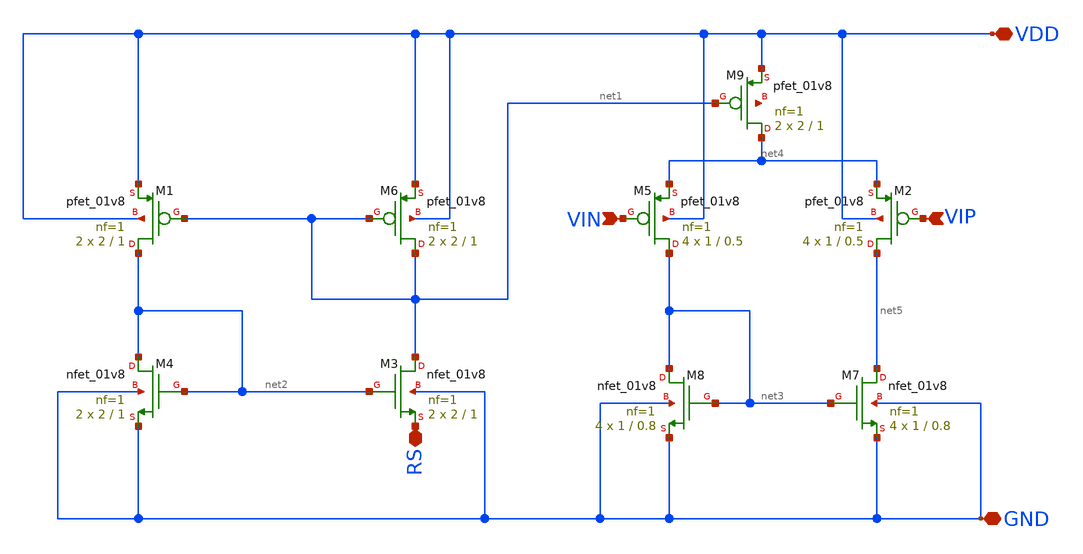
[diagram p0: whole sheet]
** sch_path: opamp/xschem/opamp.sch
**.subckt opamp GND VIP VIN RS VDD
*.iopin GND
*.ipin VIP
*.ipin VIN
*.iopin RS
*.iopin VDD
XM1 net2 net1 VDD VDD sky130_fd_pr__pfet_01v8 L=1 W=2 nf=1 ad='int((nf+1)/2) * W/nf * 0.29' as='int((nf+2)/2) * W/nf * 0.29'
+ pd='2*int((nf+1)/2) * (W/nf + 0.29)' ps='2*int((nf+2)/2) * (W/nf + 0.29)' nrd='0.29 / W' nrs='0.29 / W'
+ sa=0 sb=0 sd=0 mult=2 m=2
XM2 net5 VIP net4 VDD sky130_fd_pr__pfet_01v8 L=0.5 W=1 nf=1 ad='int((nf+1)/2) * W/nf * 0.29' as='int((nf+2)/2) * W/nf * 0.29'
+ pd='2*int((nf+1)/2) * (W/nf + 0.29)' ps='2*int((nf+2)/2) * (W/nf + 0.29)' nrd='0.29 / W' nrs='0.29 / W'
+ sa=0 sb=0 sd=0 mult=4 m=4
XM3 net1 net2 RS GND sky130_fd_pr__nfet_01v8 L=1 W=2 nf=1 ad='int((nf+1)/2) * W/nf * 0.29' as='int((nf+2)/2) * W/nf * 0.29'
+ pd='2*int((nf+1)/2) * (W/nf + 0.29)' ps='2*int((nf+2)/2) * (W/nf + 0.29)' nrd='0.29 / W' nrs='0.29 / W'
+ sa=0 sb=0 sd=0 mult=2 m=2
XM4 net2 net2 GND GND sky130_fd_pr__nfet_01v8 L=1 W=2 nf=1 ad='int((nf+1)/2) * W/nf * 0.29' as='int((nf+2)/2) * W/nf * 0.29'
+ pd='2*int((nf+1)/2) * (W/nf + 0.29)' ps='2*int((nf+2)/2) * (W/nf + 0.29)' nrd='0.29 / W' nrs='0.29 / W'
+ sa=0 sb=0 sd=0 mult=2 m=2
XM5 net3 VIN net4 VDD sky130_fd_pr__pfet_01v8 L=0.5 W=1 nf=1 ad='int((nf+1)/2) * W/nf * 0.29' as='int((nf+2)/2) * W/nf * 0.29'
+ pd='2*int((nf+1)/2) * (W/nf + 0.29)' ps='2*int((nf+2)/2) * (W/nf + 0.29)' nrd='0.29 / W' nrs='0.29 / W'
+ sa=0 sb=0 sd=0 mult=4 m=4
XM6 net1 net1 VDD VDD sky130_fd_pr__pfet_01v8 L=1 W=2 nf=1 ad='int((nf+1)/2) * W/nf * 0.29' as='int((nf+2)/2) * W/nf * 0.29'
+ pd='2*int((nf+1)/2) * (W/nf + 0.29)' ps='2*int((nf+2)/2) * (W/nf + 0.29)' nrd='0.29 / W' nrs='0.29 / W'
+ sa=0 sb=0 sd=0 mult=2 m=2
XM7 net5 net3 GND GND sky130_fd_pr__nfet_01v8 L=0.8 W=1 nf=1 ad='int((nf+1)/2) * W/nf * 0.29' as='int((nf+2)/2) * W/nf * 0.29'
+ pd='2*int((nf+1)/2) * (W/nf + 0.29)' ps='2*int((nf+2)/2) * (W/nf + 0.29)' nrd='0.29 / W' nrs='0.29 / W'
+ sa=0 sb=0 sd=0 mult=4 m=4
XM8 net3 net3 GND GND sky130_fd_pr__nfet_01v8 L=0.8 W=1 nf=1 ad='int((nf+1)/2) * W/nf * 0.29' as='int((nf+2)/2) * W/nf * 0.29'
+ pd='2*int((nf+1)/2) * (W/nf + 0.29)' ps='2*int((nf+2)/2) * (W/nf + 0.29)' nrd='0.29 / W' nrs='0.29 / W'
+ sa=0 sb=0 sd=0 mult=4 m=4
XM9 net4 net1 VDD net6 sky130_fd_pr__pfet_01v8 L=1 W=2 nf=1 ad='int((nf+1)/2) * W/nf * 0.29' as='int((nf+2)/2) * W/nf * 0.29'
+ pd='2*int((nf+1)/2) * (W/nf + 0.29)' ps='2*int((nf+2)/2) * (W/nf + 0.29)' nrd='0.29 / W' nrs='0.29 / W'
+ sa=0 sb=0 sd=0 mult=2 m=2
**.ends
.end
